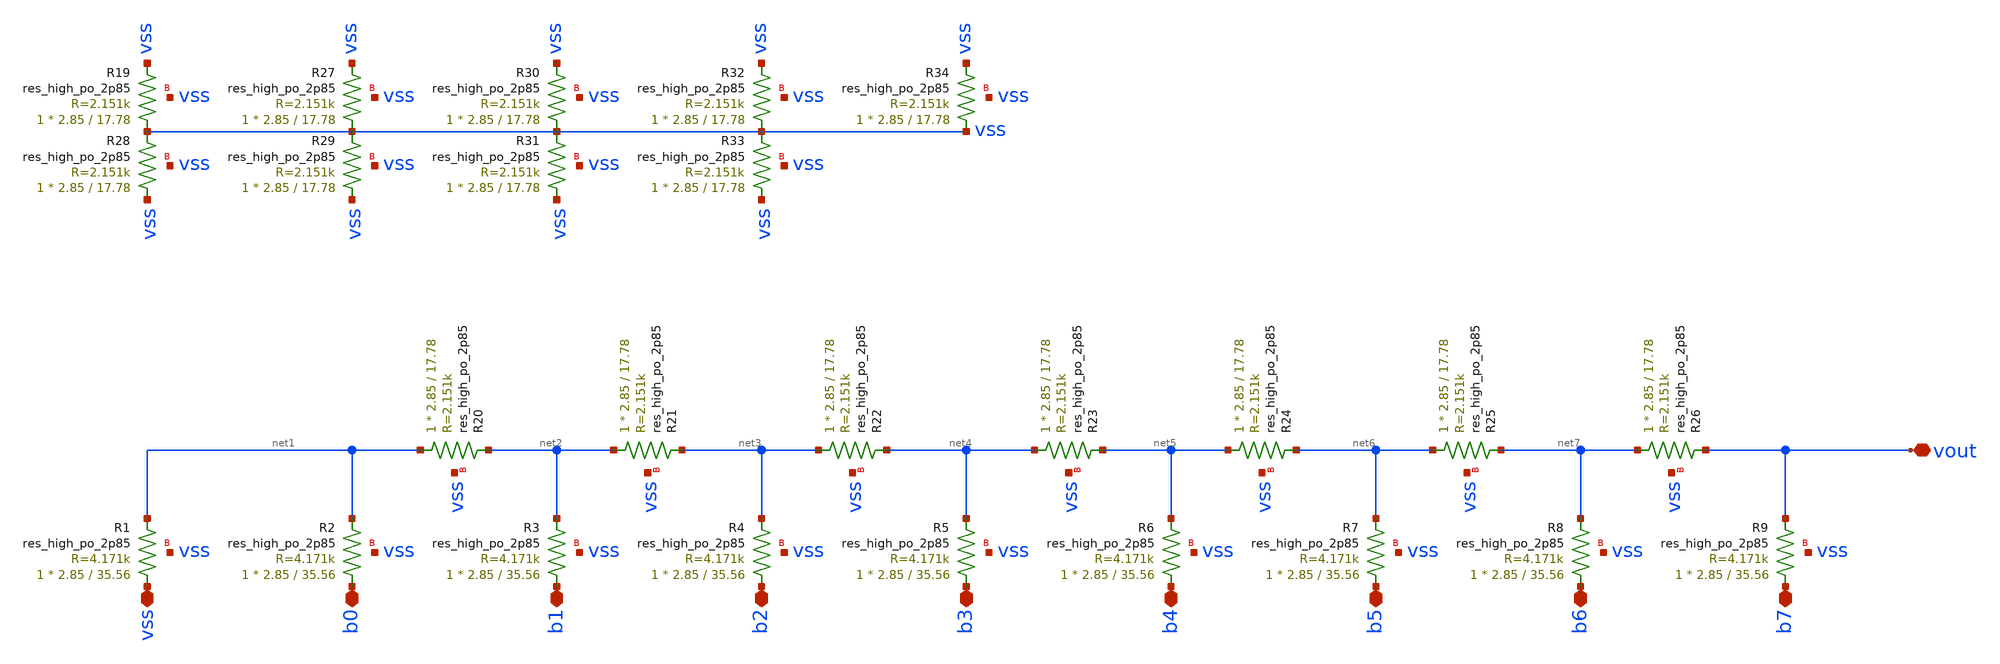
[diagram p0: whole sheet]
** sch_path: xschem/r2r_8.sch
**.subckt r2r_8 b0 vss vout b1 b2 b3 b4 b5 b6 b7
*.iopin b0
*.iopin vss
*.iopin vout
*.iopin b1
*.iopin b2
*.iopin b3
*.iopin b4
*.iopin b5
*.iopin b6
*.iopin b7
XR20 net1 net2 vss sky130_fd_pr__res_high_po_2p85 L=17.78 mult=1 m=1
XR21 net2 net3 vss sky130_fd_pr__res_high_po_2p85 L=17.78 mult=1 m=1
XR22 net3 net4 vss sky130_fd_pr__res_high_po_2p85 L=17.78 mult=1 m=1
XR23 net4 net5 vss sky130_fd_pr__res_high_po_2p85 L=17.78 mult=1 m=1
XR24 net5 net6 vss sky130_fd_pr__res_high_po_2p85 L=17.78 mult=1 m=1
XR25 net6 net7 vss sky130_fd_pr__res_high_po_2p85 L=17.78 mult=1 m=1
XR26 net7 vout vss sky130_fd_pr__res_high_po_2p85 L=17.78 mult=1 m=1
XR19 vss vss vss sky130_fd_pr__res_high_po_2p85 L=17.78 mult=1 m=1
XR27 vss vss vss sky130_fd_pr__res_high_po_2p85 L=17.78 mult=1 m=1
XR28 vss vss vss sky130_fd_pr__res_high_po_2p85 L=17.78 mult=1 m=1
XR29 vss vss vss sky130_fd_pr__res_high_po_2p85 L=17.78 mult=1 m=1
XR30 vss vss vss sky130_fd_pr__res_high_po_2p85 L=17.78 mult=1 m=1
XR31 vss vss vss sky130_fd_pr__res_high_po_2p85 L=17.78 mult=1 m=1
XR32 vss vss vss sky130_fd_pr__res_high_po_2p85 L=17.78 mult=1 m=1
XR33 vss vss vss sky130_fd_pr__res_high_po_2p85 L=17.78 mult=1 m=1
XR34 vss vss vss sky130_fd_pr__res_high_po_2p85 L=17.78 mult=1 m=1
XR1 vss net1 vss sky130_fd_pr__res_high_po_2p85 L=35.56 mult=1 m=1
XR2 b0 net1 vss sky130_fd_pr__res_high_po_2p85 L=35.56 mult=1 m=1
XR3 b1 net2 vss sky130_fd_pr__res_high_po_2p85 L=35.56 mult=1 m=1
XR4 b2 net3 vss sky130_fd_pr__res_high_po_2p85 L=35.56 mult=1 m=1
XR5 b3 net4 vss sky130_fd_pr__res_high_po_2p85 L=35.56 mult=1 m=1
XR6 b4 net5 vss sky130_fd_pr__res_high_po_2p85 L=35.56 mult=1 m=1
XR7 b5 net6 vss sky130_fd_pr__res_high_po_2p85 L=35.56 mult=1 m=1
XR8 b6 net7 vss sky130_fd_pr__res_high_po_2p85 L=35.56 mult=1 m=1
XR9 b7 vout vss sky130_fd_pr__res_high_po_2p85 L=35.56 mult=1 m=1
**.ends
.end
